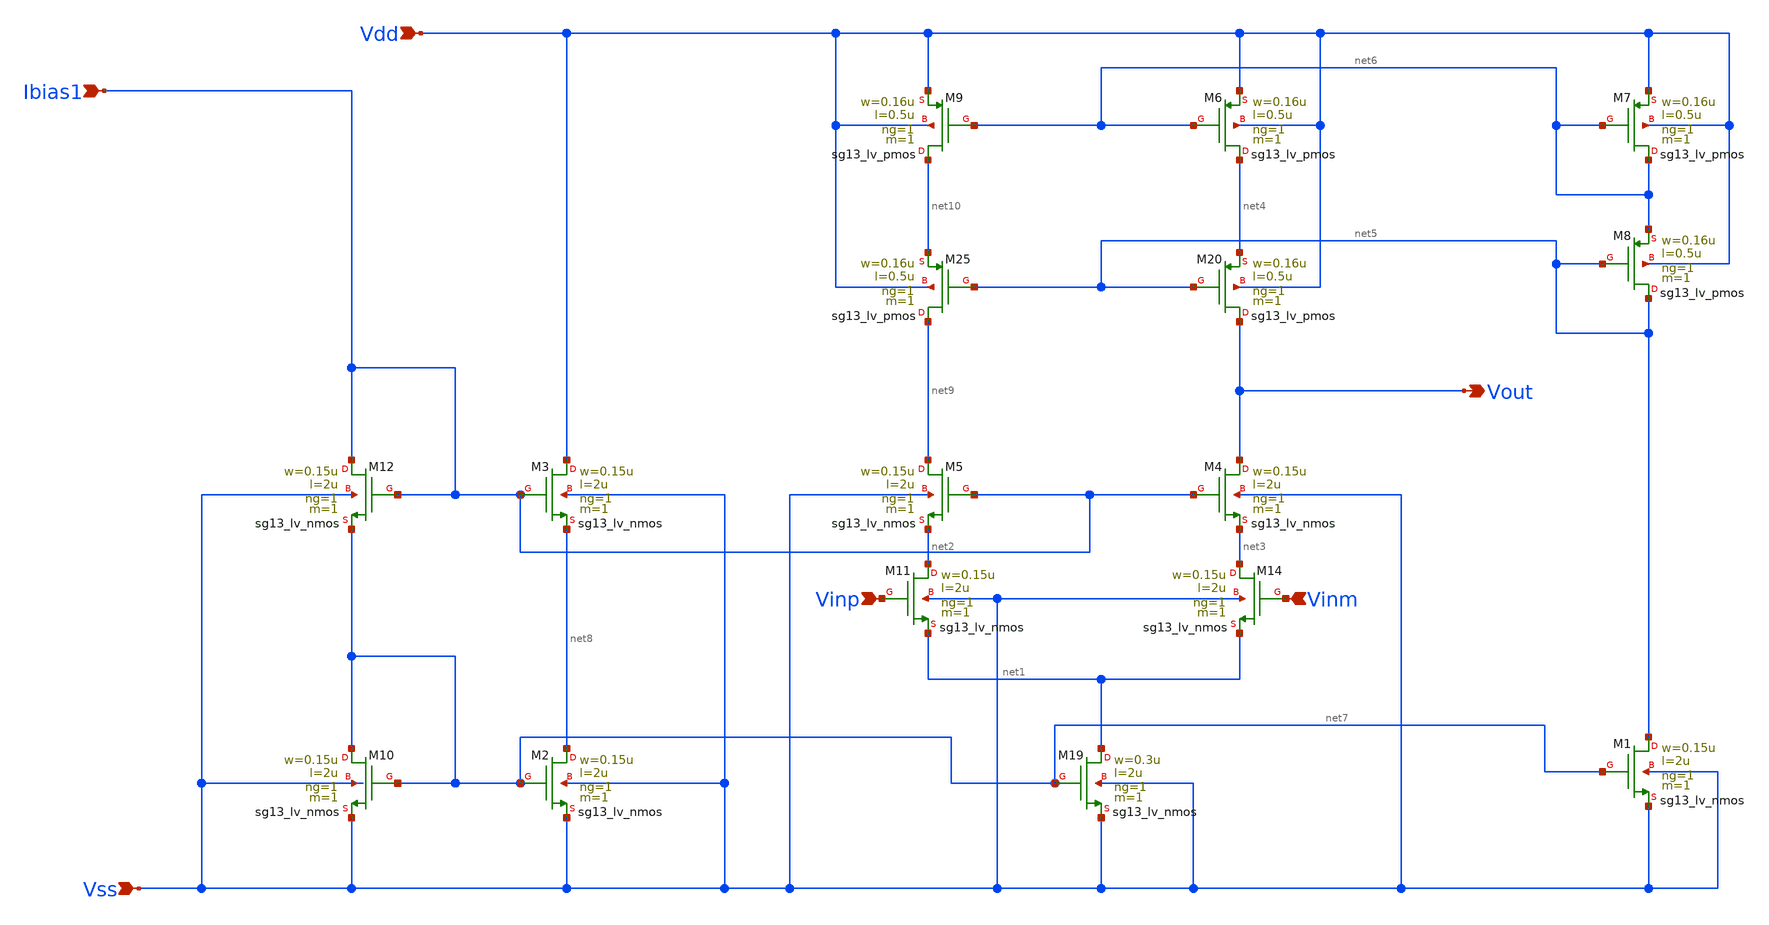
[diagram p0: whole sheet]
** sch_path: DSM/Schematics/Designs_Hrishi/RealCircuits/Telescopic/Telescopic.sch
* (c) 2024 Hrishikesh, @HSB
**.subckt Telescopic Vinp Vout Vinm Vss Vdd Ibias1
*.ipin Vinp
*.opin Vout
*.ipin Vinm
*.ipin Vss
*.ipin Vdd
*.ipin Ibias1
XM19 net1 net7 Vss Vss sg13_lv_nmos w=0.3u l=2u ng=1 m=1 mm_ok=1
XM11 net2 Vinp net1 Vss sg13_lv_nmos w=0.15u l=2u ng=1 m=1 mm_ok=1
XM14 net3 Vinm net1 Vss sg13_lv_nmos w=0.15u l=2u ng=1 m=1 mm_ok=1
XM20 Vout net5 net4 Vdd sg13_lv_pmos w=0.16u l=0.5u ng=1 m=1 mm_ok=1
XM25 net9 net5 net10 Vdd sg13_lv_pmos w=0.16u l=0.5u ng=1 m=1 mm_ok=1
XM1 net5 net7 Vss Vss sg13_lv_nmos w=0.15u l=2u ng=1 m=1 mm_ok=1
XM2 net8 net7 Vss Vss sg13_lv_nmos w=0.15u l=2u ng=1 m=1 mm_ok=1
XM3 Vdd Ibias1 net8 Vss sg13_lv_nmos w=0.15u l=2u ng=1 m=1 mm_ok=1
XM4 Vout Ibias1 net3 Vss sg13_lv_nmos w=0.15u l=2u ng=1 m=1 mm_ok=1
XM5 net9 Ibias1 net2 Vss sg13_lv_nmos w=0.15u l=2u ng=1 m=1 mm_ok=1
XM6 net4 net6 Vdd Vdd sg13_lv_pmos w=0.16u l=0.5u ng=1 m=1 mm_ok=1
XM7 net6 net6 Vdd Vdd sg13_lv_pmos w=0.16u l=0.5u ng=1 m=1 mm_ok=1
XM8 net5 net5 net6 Vdd sg13_lv_pmos w=0.16u l=0.5u ng=1 m=1 mm_ok=1
XM9 net10 net6 Vdd Vdd sg13_lv_pmos w=0.16u l=0.5u ng=1 m=1 mm_ok=1
XM10 net7 net7 Vss Vss sg13_lv_nmos w=0.15u l=2u ng=1 m=1 mm_ok=1
XM12 Ibias1 Ibias1 net7 Vss sg13_lv_nmos w=0.15u l=2u ng=1 m=1 mm_ok=1
**.ends
.end
